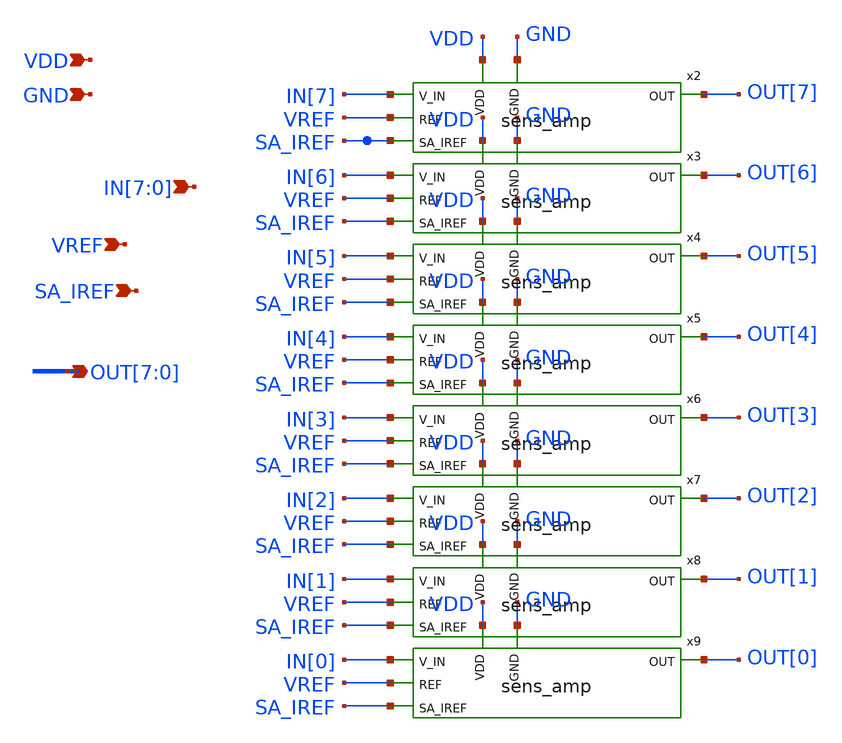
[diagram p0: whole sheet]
** sch_path: xschem/8bit_SA.sch
**.subckt 8bit_SA IN[7],IN[6],IN[5],IN[4],IN[3],IN[2],IN[1],IN[0] VREF
*+ OUT[7],OUT[6],OUT[5],OUT[4],OUT[3],OUT[2],OUT[1],OUT[0] SA_IREF VDD GND
*.ipin IN[7],IN[6],IN[5],IN[4],IN[3],IN[2],IN[1],IN[0]
*.ipin VREF
*.opin OUT[7],OUT[6],OUT[5],OUT[4],OUT[3],OUT[2],OUT[1],OUT[0]
*.ipin SA_IREF
*.ipin VDD
*.ipin GND
x2 OUT[7] VREF IN[7] SA_IREF VDD GND sens_amp
x3 OUT[6] VREF IN[6] SA_IREF VDD GND sens_amp
x4 OUT[5] VREF IN[5] SA_IREF VDD GND sens_amp
x5 OUT[4] VREF IN[4] SA_IREF VDD GND sens_amp
x6 OUT[3] VREF IN[3] SA_IREF VDD GND sens_amp
x7 OUT[2] VREF IN[2] SA_IREF VDD GND sens_amp
x8 OUT[1] VREF IN[1] SA_IREF VDD GND sens_amp
x9 OUT[0] VREF IN[0] SA_IREF VDD GND sens_amp
**.ends

* expanding   symbol:  sens_amp.sym # of pins=6
** sym_path: xschem/sens_amp.sym
** sch_path: xschem/sens_amp.sch
.subckt sens_amp OUT REF V_IN SA_IREF VDD GND
*.ipin REF
*.ipin V_IN
*.opin OUT
*.ipin SA_IREF
*.ipin VDD
*.ipin GND
XM5 net1 GN VDD VDD sky130_fd_pr__pfet_01v8_lvt L=0.5 W=1 nf=1 ad='W * 0.29' as='W * 0.29' pd='2*(W + 0.29)'
+ ps='2*(W + 0.29)' nrd=0 nrs=0 sa=0 sb=0 sd=0 mult=1 m=1
XM6 GN GN VDD VDD sky130_fd_pr__pfet_01v8_lvt L=0.5 W=1 nf=1 ad='W * 0.29' as='W * 0.29' pd='2*(W + 0.29)'
+ ps='2*(W + 0.29)' nrd=0 nrs=0 sa=0 sb=0 sd=0 mult=1 m=1
XM23 net1 V_IN net2 GND sky130_fd_pr__nfet_01v8_lvt L=0.15 W=4 nf=1 ad='W * 0.29' as='W * 0.29' pd='2*(W + 0.29)'
+ ps='2*(W + 0.29)' nrd=0 nrs=0 sa=0 sb=0 sd=0 mult=1 m=1
XM16 GN REF net2 GND sky130_fd_pr__nfet_01v8_lvt L=0.15 W=4 nf=1 ad='W * 0.29' as='W * 0.29' pd='2*(W + 0.29)'
+ ps='2*(W + 0.29)' nrd=0 nrs=0 sa=0 sb=0 sd=0 mult=1 m=1
XM1 OUT net1 GND GND sky130_fd_pr__nfet_01v8_lvt L=0.15 W=1 nf=1 ad='W * 0.29' as='W * 0.29' pd='2*(W + 0.29)'
+ ps='2*(W + 0.29)' nrd=0 nrs=0 sa=0 sb=0 sd=0 mult=1 m=1
XM2 OUT net1 VDD VDD sky130_fd_pr__pfet_01v8_lvt L=0.35 W=3 nf=1 ad='W * 0.29' as='W * 0.29' pd='2*(W + 0.29)'
+ ps='2*(W + 0.29)' nrd=0 nrs=0 sa=0 sb=0 sd=0 mult=1 m=1
XM3 net2 SA_IREF GND GND sky130_fd_pr__nfet_01v8_lvt L=1 W=0.5 nf=1 ad='W * 0.29' as='W * 0.29' pd='2*(W + 0.29)'
+ ps='2*(W + 0.29)' nrd=0 nrs=0 sa=0 sb=0 sd=0 mult=1 m=1
.ends

.GLOBAL GND
.end
